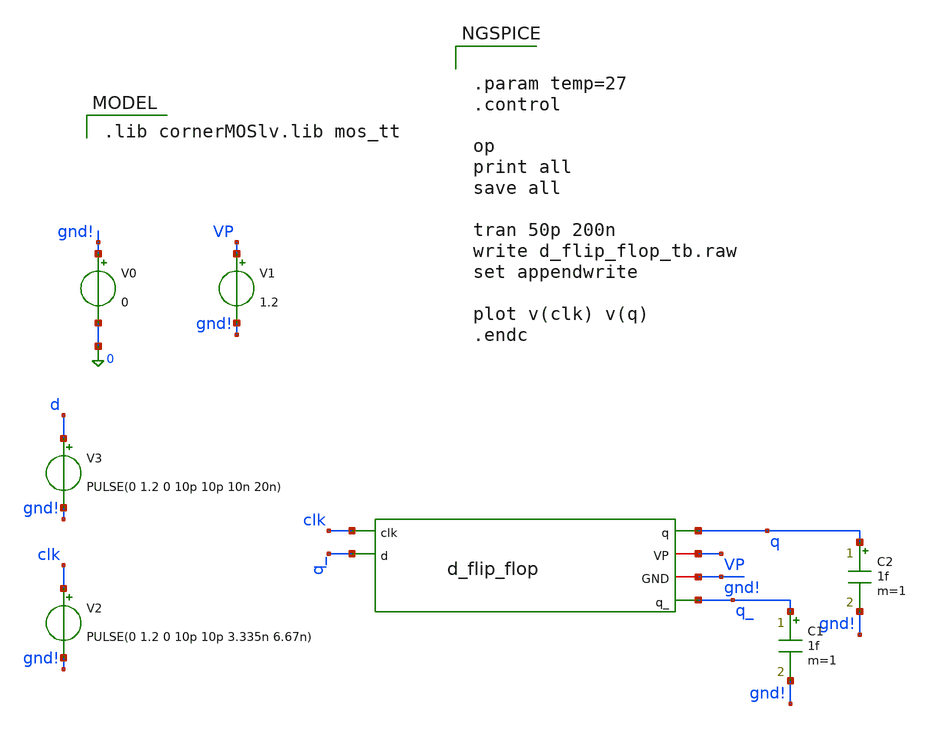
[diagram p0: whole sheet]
** sch_path: divider/d_flip_flop_tb.sch
**.subckt d_flip_flop_tb
x1 q VP gnd! q_ clk q_ d_flip_flop
V1 VP gnd! 1.2
V2 clk gnd! PULSE(0 1.2 0 10p 10p 3.335n 6.67n)
C1 q_ gnd! 1f m=1
V0 gnd! 0 0
C2 q gnd! 1f m=1
V3 d gnd! PULSE(0 1.2 0 10p 10p 10n 20n)
**** begin user architecture code
 .lib cornerMOSlv.lib mos_tt



.param temp=27
.control

op
print all
save all

tran 50p 200n
write d_flip_flop_tb.raw
set appendwrite

plot v(clk) v(q)
.endc


**** end user architecture code
**.ends
.end
